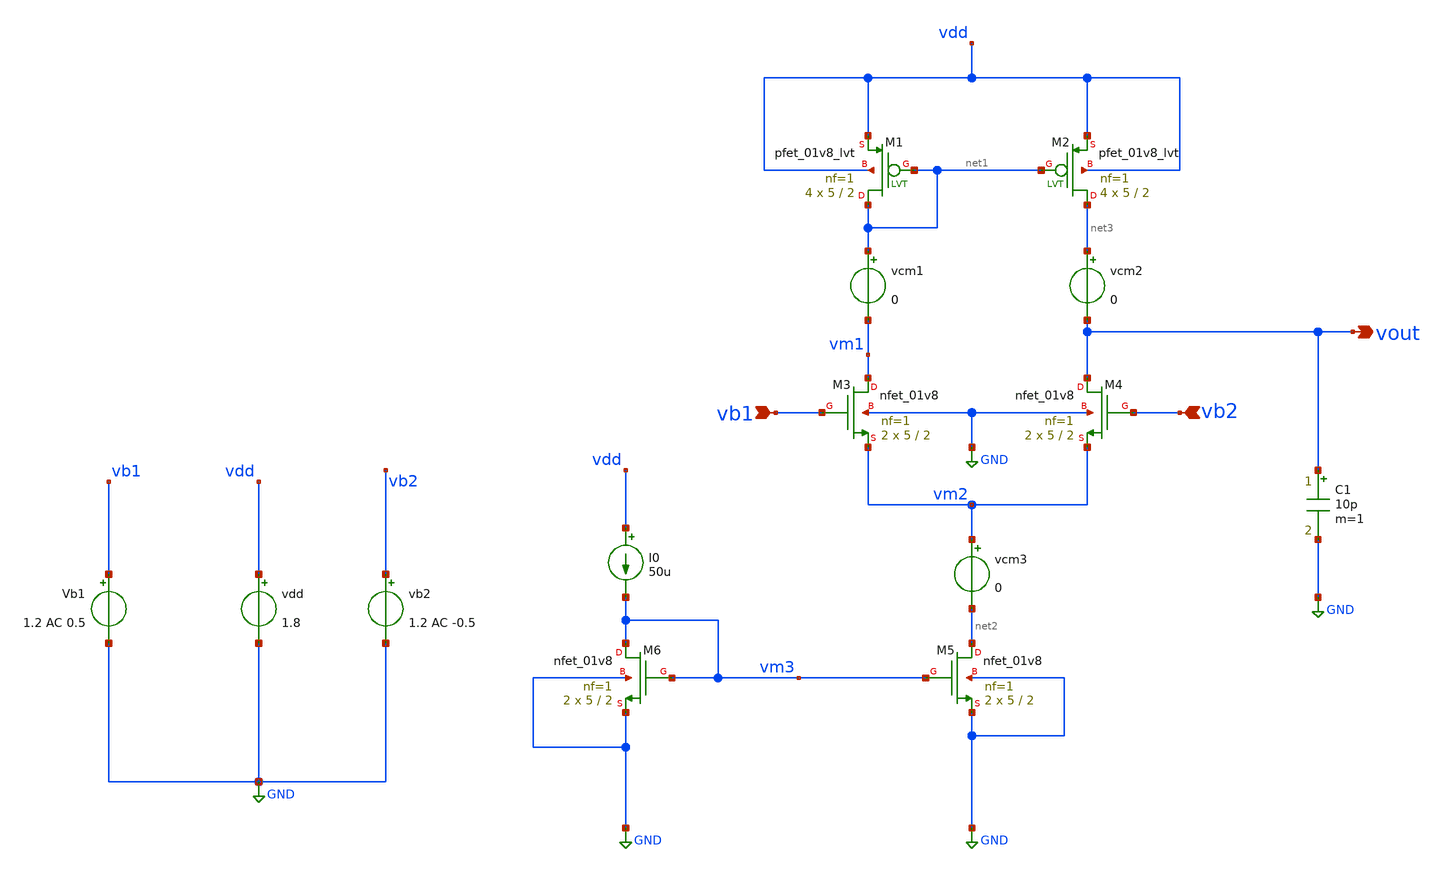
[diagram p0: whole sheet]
** sch_path: testbenches/Differential_Amplifier_AC_analysis.sch
**.subckt Differential_Amplifier_AC_analysis vout vb1 vb2
*.opin vout
*.ipin vb1
*.ipin vb2
XM5 net2 vm3 GND GND sky130_fd_pr__nfet_01v8 L=2 W=5 nf=1 ad='int((1 + 1)/2) * 5 / 1 * 0.29' as='int((1 + 2)/2) * 5 / 1 * 0.29'
+ pd='2*int((1 + 1)/2) * (5 / 1 + 0.29)' ps='2*int((1 + 2)/2) * (5 / 1 + 0.29)' nrd='0.29 / 5 ' nrs='0.29 / 5 '
+ sa=0 sb=0 sd=0 mult=2 m=2
I0 vdd vm3 50u
vdd vdd GND 1.8
Vb1 vb1 GND 1.2 AC 0.5
XM2 net3 net1 vdd vdd sky130_fd_pr__pfet_01v8_lvt L=2 W=5 nf=1 ad='int((1 + 1)/2) * 5 / 1 * 0.29' as='int((1 + 2)/2) * 5 / 1 * 0.29'
+ pd='2*int((1 + 1)/2) * (5 / 1 + 0.29)' ps='2*int((1 + 2)/2) * (5 / 1 + 0.29)' nrd='0.29 / 5 ' nrs='0.29 / 5 '
+ sa=0 sb=0 sd=0 mult=4 m=4
XM3 vm1 vb1 vm2 GND sky130_fd_pr__nfet_01v8 L=2 W=5 nf=1 ad='int((1 + 1)/2) * 5 / 1 * 0.29' as='int((1 + 2)/2) * 5 / 1 * 0.29'
+ pd='2*int((1 + 1)/2) * (5 / 1 + 0.29)' ps='2*int((1 + 2)/2) * (5 / 1 + 0.29)' nrd='0.29 / 5 ' nrs='0.29 / 5 '
+ sa=0 sb=0 sd=0 mult=2 m=2
XM4 vout vb2 vm2 GND sky130_fd_pr__nfet_01v8 L=2 W=5 nf=1 ad='int((1 + 1)/2) * 5 / 1 * 0.29' as='int((1 + 2)/2) * 5 / 1 * 0.29'
+ pd='2*int((1 + 1)/2) * (5 / 1 + 0.29)' ps='2*int((1 + 2)/2) * (5 / 1 + 0.29)' nrd='0.29 / 5 ' nrs='0.29 / 5 '
+ sa=0 sb=0 sd=0 mult=2 m=2
XM6 vm3 vm3 GND GND sky130_fd_pr__nfet_01v8 L=2 W=5 nf=1 ad='int((1 + 1)/2) * 5 / 1 * 0.29' as='int((1 + 2)/2) * 5 / 1 * 0.29'
+ pd='2*int((1 + 1)/2) * (5 / 1 + 0.29)' ps='2*int((1 + 2)/2) * (5 / 1 + 0.29)' nrd='0.29 / 5 ' nrs='0.29 / 5 '
+ sa=0 sb=0 sd=0 mult=2 m=2
XM1 net1 net1 vdd vdd sky130_fd_pr__pfet_01v8_lvt L=2 W=5 nf=1 ad='int((1 + 1)/2) * 5 / 1 * 0.29' as='int((1 + 2)/2) * 5 / 1 * 0.29'
+ pd='2*int((1 + 1)/2) * (5 / 1 + 0.29)' ps='2*int((1 + 2)/2) * (5 / 1 + 0.29)' nrd='0.29 / 5 ' nrs='0.29 / 5 '
+ sa=0 sb=0 sd=0 mult=4 m=4
vcm3 vm2 net2 0
vcm1 net1 vm1 0
vcm2 net3 vout 0
C1 vout GND 10p m=1
vb2 vb2 GND 1.2 AC -0.5
**** begin user architecture code

** opencircuitdesign pdks install
.lib $::SKYWATER_MODELS/sky130.lib.spice tt




.ac dec 10 1 10G

.control
run
save all

set color0 = white

* Plot gain and phase
plot db(v(vout)) title 'Magnitude Response (Gain in dB)'
plot ph(v(vout))*(180/pi)

* Low-frequency gain (at first AC point)
let gain0 = db(v(vout))[0]


* 3-dB Bandwidth
meas ac BW_3DB when db(v(vout))=(gain0-3)

* Unity Gain Bandwidth (0 dB crossing)
meas ac UGB when db(v(vout))=0

.endc



**** end user architecture code
**.ends
.GLOBAL GND
.end
